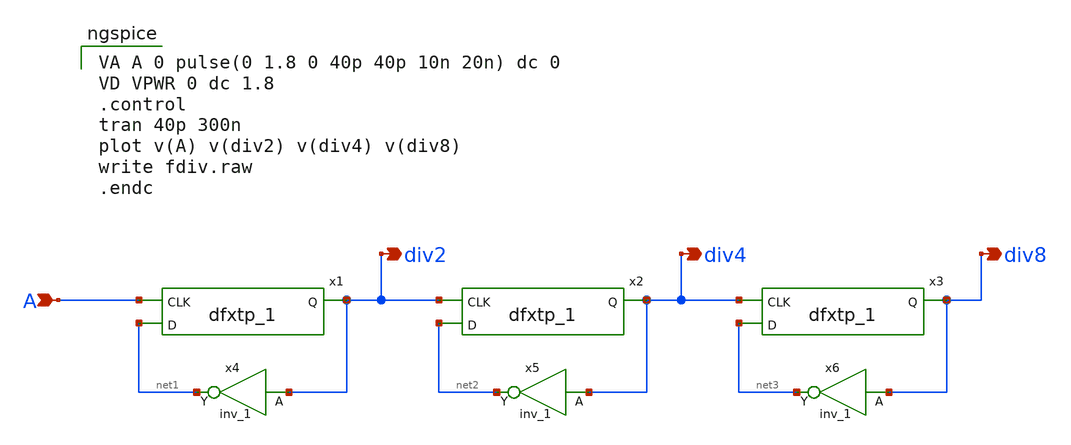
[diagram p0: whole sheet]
** sch_path: fdiv.sch
**.subckt fdiv div2 A div4 div8
*.opin div2
*.ipin A
*.opin div4
*.opin div8
x1 A net1 0 0 VPWR VPWR div2 sky130_fd_sc_hd__dfxtp_1
x4 div2 0 0 VPWR VPWR net1 sky130_fd_sc_hd__inv_1
x2 div2 net2 0 0 VPWR VPWR div4 sky130_fd_sc_hd__dfxtp_1
x3 div4 net3 0 0 VPWR VPWR div8 sky130_fd_sc_hd__dfxtp_1
x5 div4 0 0 VPWR VPWR net2 sky130_fd_sc_hd__inv_1
x6 div8 0 0 VPWR VPWR net3 sky130_fd_sc_hd__inv_1
**** begin user architecture code

VA A 0 pulse(0 1.8 0 40p 40p 10n 20n) dc 0
VD VPWR 0 dc 1.8
.control
tran 40p 300n
plot v(A) v(div2) v(div4) v(div8)
write fdiv.raw
.endc


** opencircuitdesign pdks install
.lib $::SKYWATER_MODELS/sky130.lib.spice tt
.include $::SKYWATER_STDCELLS/sky130_fd_sc_hd.spice

**** end user architecture code
**.ends
.end
